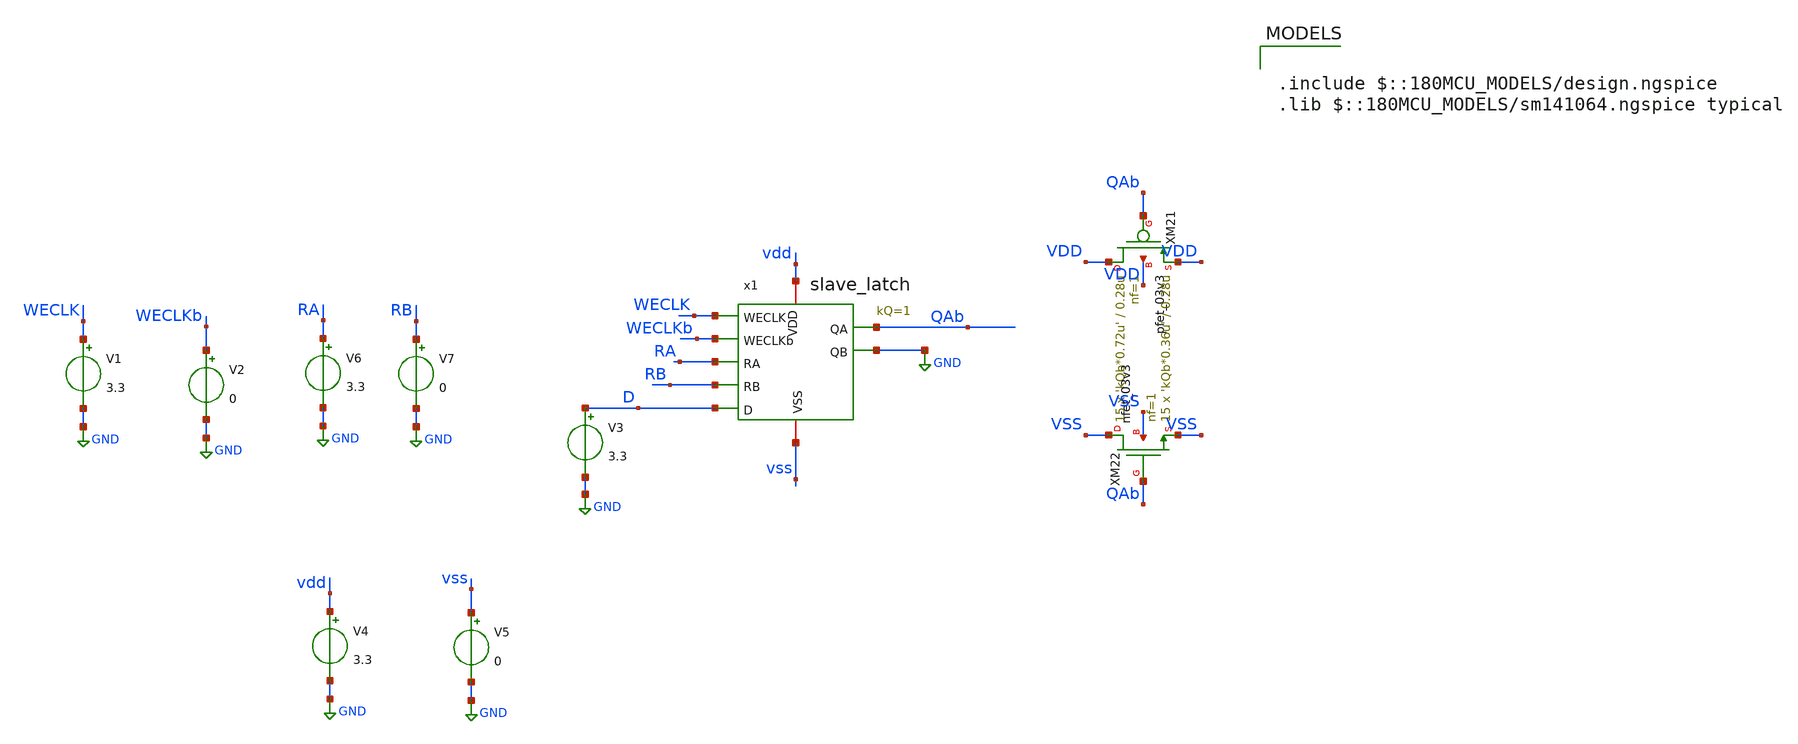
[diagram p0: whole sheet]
** sch_path: CAD3/slave_latch_sizing_martin.sch
**.subckt slave_latch_sizing_martin
V1 WECLK GND 3.3
V3 D GND 3.3
V2 WECLKb GND 0
V4 vdd GND 3.3
V5 vss GND 0
x1 vdd vss QAb WECLK WECLKb RA RB GND D slave_latch kQ=1
V6 RA GND 3.3
V7 RB GND 0
XM21 VDD QAb VDD VDD pfet_03v3 L=0.28u W='kQb*0.72u' nf=1 ad='int((nf+1)/2) * W/nf * 0.18u' as='int((nf+2)/2) * W/nf * 0.18u'
+ pd='2*int((nf+1)/2) * (W/nf + 0.18u)' ps='2*int((nf+2)/2) * (W/nf + 0.18u)' nrd='0.18u / W' nrs='0.18u / W'
+ sa=0 sb=0 sd=0 m=15
XM22 VSS QAb VSS VSS nfet_03v3 L=0.28u W='kQb*0.36u' nf=1 ad='int((nf+1)/2) * W/nf * 0.18u' as='int((nf+2)/2) * W/nf * 0.18u'
+ pd='2*int((nf+1)/2) * (W/nf + 0.18u)' ps='2*int((nf+2)/2) * (W/nf + 0.18u)' nrd='0.18u / W' nrs='0.18u / W'
+ sa=0 sb=0 sd=0 m=15
**** begin user architecture code

.include $::180MCU_MODELS/design.ngspice
.lib $::180MCU_MODELS/sm141064.ngspice typical




.param kQb = 1
.control
save all

let fsig = 1e8
let tper = 1/fsig
let tfr = 0.01*tper
let ton = 0.5*tper - 2*tfr

let tstop = 3*tper
let tstep = 0.001 * tper

let Rvals = vector(20)
let rise_times = vector(20)
let i = 0

let rval = 1
let Rstep = 0.2
let Rstop = 5

while rval <= Rstop

	alterparam kQb = $&rval
	reset

	* WECLK pulse
	alter @v1[DC] = 0
	alter @v1[PULSE] = [ 0 3.3 1n $&tfr $&tfr $&ton $&tper 0 ]

	*WECLKb pulse
	alter @v2[DC] = 0
	alter @v2[PULSE] = [ 3.3 0 1n $&tfr $&tfr $&ton $&tper 0 ]

	*RA pulse
	alter @v6[DC] = 0
	alter @v6[PULSE] = [ 0 3.3 3.03n $&tfr $&tfr $&ton $&tper 0 ]

	*D pulse
	*rising alter @v3[PWL] = [ 0 3.3 8n 3.3 8.001n 0 ]
	alter @v3[PWL] = [ 0 0 8n 3.3 8.001n 3.3 ]



	tran $&tstep $&tstop

	meas tran t1 TRIG V(RA) VAL=1.65 RISE=2 TARG V(QAb) VAL=1.5 FALL=1

	let Rvals[i] = rval
	let rise_times[i] = t1
	let rval = rval + Rstep
	let i = i + 1

	echo kQb=$&rval t1=$&t1
end
.endc



**** end user architecture code
**.ends

* expanding   symbol:  engn1600-team1/CAD3/slave_latch.sym # of pins=9
** sym_path: CAD3/slave_latch.sym
** sch_path: CAD3/slave_latch.sch
.subckt slave_latch VDD VSS QA WECLK WECLKb RA RB QB D  kQ=1
*.ipin D
*.ipin RA
*.ipin RB
*.ipin WECLKb
*.ipin WECLK
*.opin QA
*.opin QB
*.iopin VDD
*.iopin VSS
XM1 net1 WECLKb net2 VDD pfet_03v3 L=0.28u W=0.22u nf=1 ad='int((nf+1)/2) * W/nf * 0.18u' as='int((nf+2)/2) * W/nf * 0.18u'
+ pd='2*int((nf+1)/2) * (W/nf + 0.18u)' ps='2*int((nf+2)/2) * (W/nf + 0.18u)' nrd='0.18u / W' nrs='0.18u / W'
+ sa=0 sb=0 sd=0 m=1
XM2 net1 D VDD VDD pfet_03v3 L=0.28u W=0.22u nf=1 ad='int((nf+1)/2) * W/nf * 0.18u' as='int((nf+2)/2) * W/nf * 0.18u'
+ pd='2*int((nf+1)/2) * (W/nf + 0.18u)' ps='2*int((nf+2)/2) * (W/nf + 0.18u)' nrd='0.18u / W' nrs='0.18u / W'
+ sa=0 sb=0 sd=0 m=1
XM3 net3 net2 VDD VDD pfet_03v3 L=0.28u W=0.22u nf=1 ad='int((nf+1)/2) * W/nf * 0.18u' as='int((nf+2)/2) * W/nf * 0.18u'
+ pd='2*int((nf+1)/2) * (W/nf + 0.18u)' ps='2*int((nf+2)/2) * (W/nf + 0.18u)' nrd='0.18u / W' nrs='0.18u / W'
+ sa=0 sb=0 sd=0 m=1
XM4 net4 net2 VDD VDD pfet_03v3 L=0.28u W=0.22u nf=1 ad='int((nf+1)/2) * W/nf * 0.18u' as='int((nf+2)/2) * W/nf * 0.18u'
+ pd='2*int((nf+1)/2) * (W/nf + 0.18u)' ps='2*int((nf+2)/2) * (W/nf + 0.18u)' nrd='0.18u / W' nrs='0.18u / W'
+ sa=0 sb=0 sd=0 m=1
XM5 VDD WECLK net8 VDD pfet_03v3 L=0.28u W=0.22u nf=1 ad='int((nf+1)/2) * W/nf * 0.18u' as='int((nf+2)/2) * W/nf * 0.18u'
+ pd='2*int((nf+1)/2) * (W/nf + 0.18u)' ps='2*int((nf+2)/2) * (W/nf + 0.18u)' nrd='0.18u / W' nrs='0.18u / W'
+ sa=0 sb=0 sd=0 m=1
XM6 net8 net4 net2 VDD pfet_03v3 L=0.28u W=0.22u nf=1 ad='int((nf+1)/2) * W/nf * 0.18u' as='int((nf+2)/2) * W/nf * 0.18u'
+ pd='2*int((nf+1)/2) * (W/nf + 0.18u)' ps='2*int((nf+2)/2) * (W/nf + 0.18u)' nrd='0.18u / W' nrs='0.18u / W'
+ sa=0 sb=0 sd=0 m=1
XM7 net1 D VSS VSS nfet_03v3 L=0.28u W=0.22u nf=1 ad='int((nf+1)/2) * W/nf * 0.18u' as='int((nf+2)/2) * W/nf * 0.18u'
+ pd='2*int((nf+1)/2) * (W/nf + 0.18u)' ps='2*int((nf+2)/2) * (W/nf + 0.18u)' nrd='0.18u / W' nrs='0.18u / W'
+ sa=0 sb=0 sd=0 m=1
XM8 net1 WECLK net2 VSS nfet_03v3 L=0.28u W=0.22u nf=1 ad='int((nf+1)/2) * W/nf * 0.18u' as='int((nf+2)/2) * W/nf * 0.18u'
+ pd='2*int((nf+1)/2) * (W/nf + 0.18u)' ps='2*int((nf+2)/2) * (W/nf + 0.18u)' nrd='0.18u / W' nrs='0.18u / W'
+ sa=0 sb=0 sd=0 m=1
XM9 net3 net2 VSS VSS nfet_03v3 L=0.28u W=0.22u nf=1 ad='int((nf+1)/2) * W/nf * 0.18u' as='int((nf+2)/2) * W/nf * 0.18u'
+ pd='2*int((nf+1)/2) * (W/nf + 0.18u)' ps='2*int((nf+2)/2) * (W/nf + 0.18u)' nrd='0.18u / W' nrs='0.18u / W'
+ sa=0 sb=0 sd=0 m=1
XM10 net4 net2 VSS VSS nfet_03v3 L=0.28u W=0.22u nf=1 ad='int((nf+1)/2) * W/nf * 0.18u' as='int((nf+2)/2) * W/nf * 0.18u'
+ pd='2*int((nf+1)/2) * (W/nf + 0.18u)' ps='2*int((nf+2)/2) * (W/nf + 0.18u)' nrd='0.18u / W' nrs='0.18u / W'
+ sa=0 sb=0 sd=0 m=1
XM11 net7 net4 net2 VSS nfet_03v3 L=0.28u W=0.22u nf=1 ad='int((nf+1)/2) * W/nf * 0.18u' as='int((nf+2)/2) * W/nf * 0.18u'
+ pd='2*int((nf+1)/2) * (W/nf + 0.18u)' ps='2*int((nf+2)/2) * (W/nf + 0.18u)' nrd='0.18u / W' nrs='0.18u / W'
+ sa=0 sb=0 sd=0 m=1
XM12 VSS WECLKb net7 VSS nfet_03v3 L=0.28u W=0.22u nf=1 ad='int((nf+1)/2) * W/nf * 0.18u' as='int((nf+2)/2) * W/nf * 0.18u'
+ pd='2*int((nf+1)/2) * (W/nf + 0.18u)' ps='2*int((nf+2)/2) * (W/nf + 0.18u)' nrd='0.18u / W' nrs='0.18u / W'
+ sa=0 sb=0 sd=0 m=1
XM13 net3 net5 QB VDD pfet_03v3 L=0.28u W=0.22u nf=1 ad='int((nf+1)/2) * W/nf * 0.18u' as='int((nf+2)/2) * W/nf * 0.18u'
+ pd='2*int((nf+1)/2) * (W/nf + 0.18u)' ps='2*int((nf+2)/2) * (W/nf + 0.18u)' nrd='0.18u / W' nrs='0.18u / W'
+ sa=0 sb=0 sd=0 m=1
XM14 net3 RB QB VSS nfet_03v3 L=0.28u W=0.22u nf=1 ad='int((nf+1)/2) * W/nf * 0.18u' as='int((nf+2)/2) * W/nf * 0.18u'
+ pd='2*int((nf+1)/2) * (W/nf + 0.18u)' ps='2*int((nf+2)/2) * (W/nf + 0.18u)' nrd='0.18u / W' nrs='0.18u / W'
+ sa=0 sb=0 sd=0 m=1
XM15 net5 RB VDD VDD pfet_03v3 L=0.28u W=0.22u nf=1 ad='int((nf+1)/2) * W/nf * 0.18u' as='int((nf+2)/2) * W/nf * 0.18u'
+ pd='2*int((nf+1)/2) * (W/nf + 0.18u)' ps='2*int((nf+2)/2) * (W/nf + 0.18u)' nrd='0.18u / W' nrs='0.18u / W'
+ sa=0 sb=0 sd=0 m=1
XM16 net5 RB VSS VSS nfet_03v3 L=0.28u W=0.22u nf=1 ad='int((nf+1)/2) * W/nf * 0.18u' as='int((nf+2)/2) * W/nf * 0.18u'
+ pd='2*int((nf+1)/2) * (W/nf + 0.18u)' ps='2*int((nf+2)/2) * (W/nf + 0.18u)' nrd='0.18u / W' nrs='0.18u / W'
+ sa=0 sb=0 sd=0 m=1
XM21 net3 net6 QA VDD pfet_03v3 L=0.28u W=0.22u nf=1 ad='int((nf+1)/2) * W/nf * 0.18u' as='int((nf+2)/2) * W/nf * 0.18u'
+ pd='2*int((nf+1)/2) * (W/nf + 0.18u)' ps='2*int((nf+2)/2) * (W/nf + 0.18u)' nrd='0.18u / W' nrs='0.18u / W'
+ sa=0 sb=0 sd=0 m=1
XM22 net3 RA QA VSS nfet_03v3 L=0.28u W=0.22u nf=1 ad='int((nf+1)/2) * W/nf * 0.18u' as='int((nf+2)/2) * W/nf * 0.18u'
+ pd='2*int((nf+1)/2) * (W/nf + 0.18u)' ps='2*int((nf+2)/2) * (W/nf + 0.18u)' nrd='0.18u / W' nrs='0.18u / W'
+ sa=0 sb=0 sd=0 m=1
XM23 net6 RA VDD VDD pfet_03v3 L=0.28u W=0.22u nf=1 ad='int((nf+1)/2) * W/nf * 0.18u' as='int((nf+2)/2) * W/nf * 0.18u'
+ pd='2*int((nf+1)/2) * (W/nf + 0.18u)' ps='2*int((nf+2)/2) * (W/nf + 0.18u)' nrd='0.18u / W' nrs='0.18u / W'
+ sa=0 sb=0 sd=0 m=1
XM24 net6 RA VSS VSS nfet_03v3 L=0.28u W=0.22u nf=1 ad='int((nf+1)/2) * W/nf * 0.18u' as='int((nf+2)/2) * W/nf * 0.18u'
+ pd='2*int((nf+1)/2) * (W/nf + 0.18u)' ps='2*int((nf+2)/2) * (W/nf + 0.18u)' nrd='0.18u / W' nrs='0.18u / W'
+ sa=0 sb=0 sd=0 m=1
.ends

.GLOBAL GND
.end
